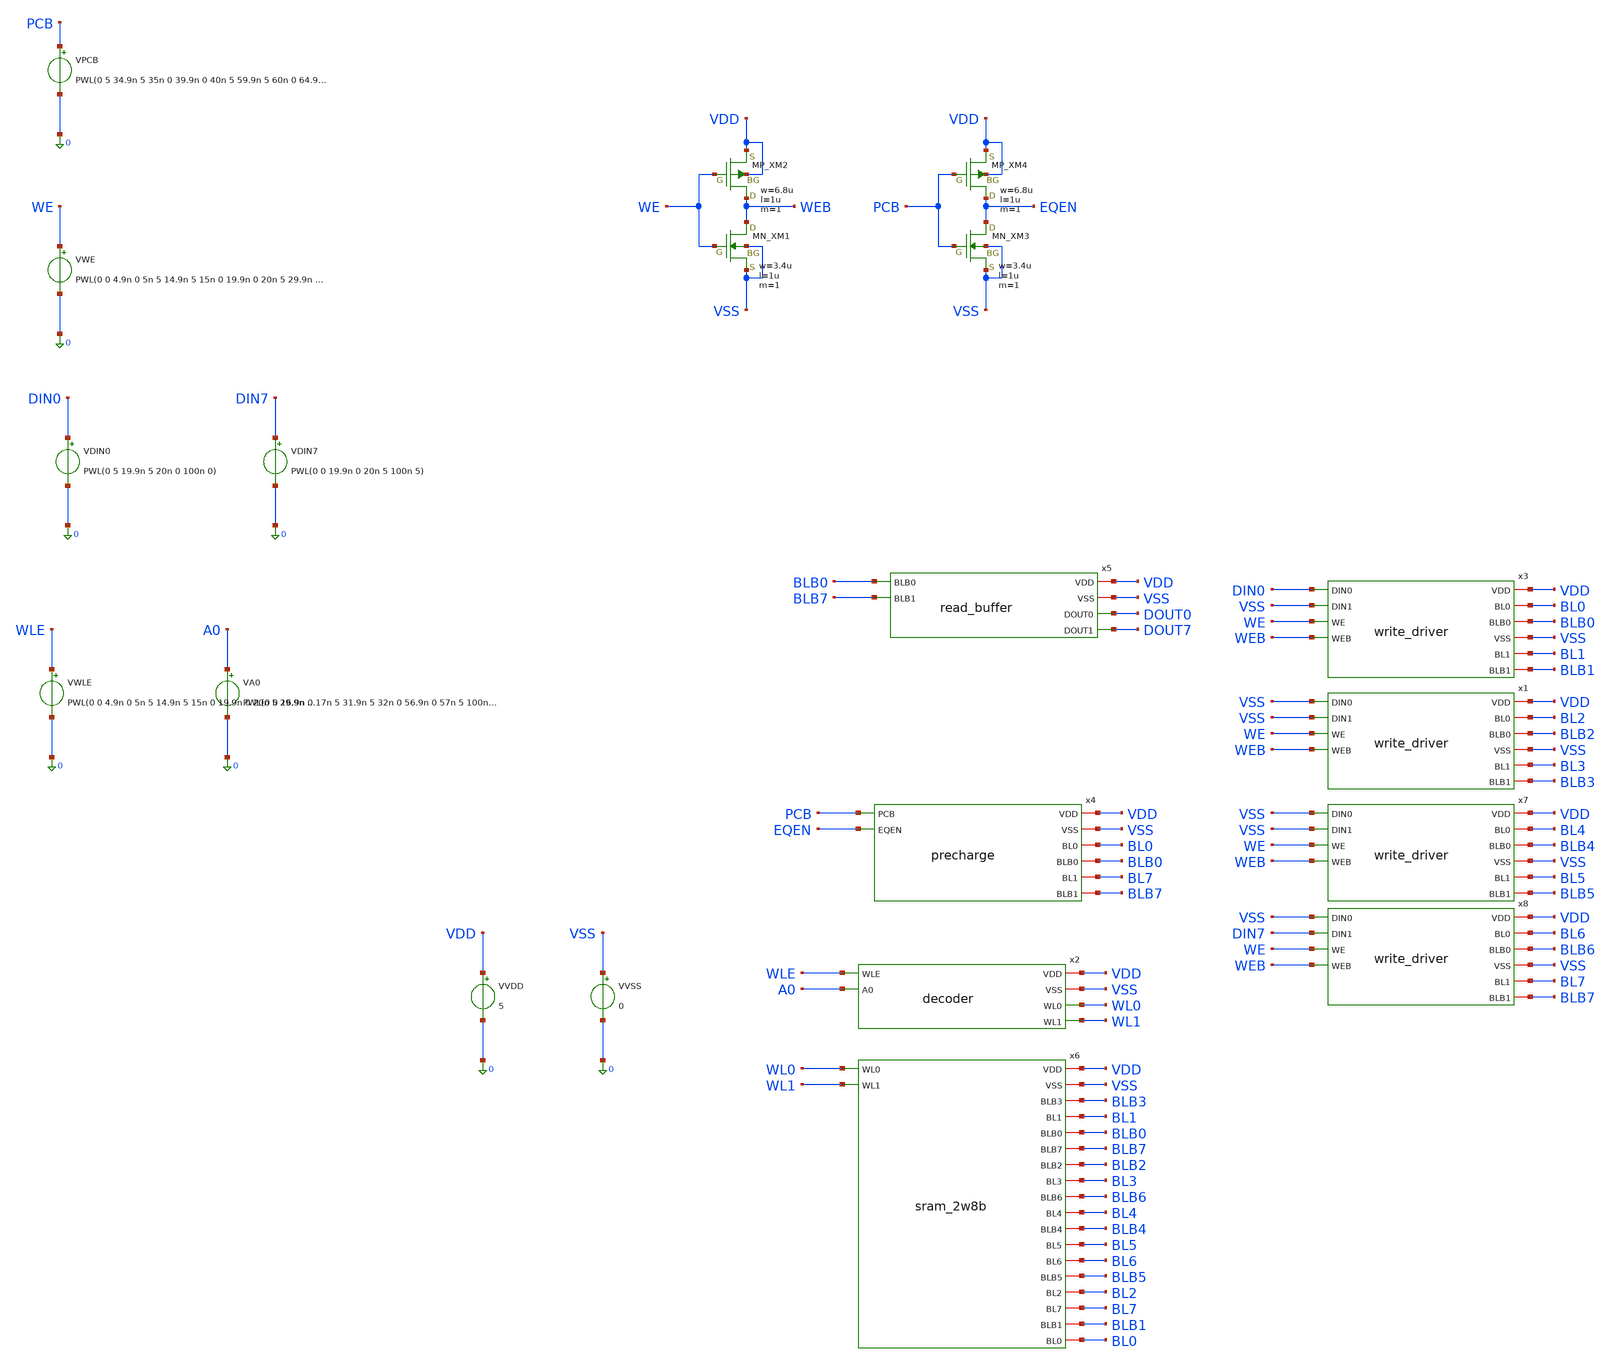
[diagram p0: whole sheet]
** sch_path: sram/tb_sram_2w8b.sch
**.subckt tb_sram_2w8b
VVDD VDD 0 5
VDIN0 DIN0 0 PWL(0 5 19.9n 5 20n 0 100n 0)
VVSS VSS 0 0
VWE WE 0 PWL(0 0 4.9n 0 5n 5 14.9n 5 15n 0 19.9n 0 20n 5 29.9n 5 30n 0 100n 0)
VPCB PCB 0 PWL(0 5 34.9n 5 35n 0 39.9n 0 40n 5 59.9n 5 60n 0 64.9n 0 65n 5 100n 5)
x2 VDD VSS WL0 WLE A0 WL1 decoder
VWLE WLE 0 PWL(0 0 4.9n 0 5n 5 14.9n 5 15n 0 19.9n 0 20n 5 29.9n 5 30n 0 44.9n 0 45n 5 54.9n 5 55n 0
+ 69.9n 0 70n 5 79.9n 5 80n 0 100n 0)
VA0 A0 0 PWL(0 0 16.9n 0 17n 5 31.9n 5 32n 0 56.9n 0 57n 5 100n 5)
x3 DIN0 VDD BL0 BLB0 VSS VSS BL1 WE BLB1 WEB write_driver
VDIN7 DIN7 0 PWL(0 0 19.9n 0 20n 5 100n 5)
x4 VDD VSS PCB EQEN BL0 BLB0 BL7 BLB7 precharge
x5 VDD VSS BLB0 BLB7 DOUT0 DOUT7 read_buffer
XXM1 WEB WE VSS VSS NMOS w=3.4u l=1u nrd=0 nrs=0 m=1
XXM2 WEB WE VDD VDD PMOS w=6.8u l=1u nrd=0 nrs=0 m=1
XXM3 EQEN PCB VSS VSS NMOS w=3.4u l=1u nrd=0 nrs=0 m=1
XXM4 EQEN PCB VDD VDD PMOS w=6.8u l=1u nrd=0 nrs=0 m=1
x6 WL0 VDD VSS WL1 BLB3 BL1 BLB0 BLB7 BLB2 BL3 BLB6 BL4 BLB4 BL5 BL6 BLB5 BL2 BL7 BLB1 BL0 sram_2w8b
x1 VSS VDD BL2 BLB2 VSS VSS BL3 WE BLB3 WEB write_driver
x7 VSS VDD BL4 BLB4 VSS VSS BL5 WE BLB5 WEB write_driver
x8 VSS VDD BL6 BLB6 VSS DIN7 BL7 WE BLB7 WEB write_driver
**** begin user architecture code
 .include $::LIB/ip62_models


.tran 10p 100n

* ============================================================
* ColMax 2w8b SRAM Read Measurement
* Observe: bit1 and bit7
* ============================================================

* WL 50% crossing
.meas tran t_wl0_rise WHEN v(WL0)=2.5 RISE=2
.meas tran t_wl1_rise WHEN v(WL1)=2.5 RISE=1

* BL differential at WL0 +0.5ns
.meas tran dvbl0_05 FIND par('abs(v(BL0)-v(BLB0))') AT=47.781n
.meas tran dvbl7_05 FIND par('abs(v(BL7)-v(BLB7))') AT=47.781n

* BL differential at WL0 +1.0ns
.meas tran dvbl0_10 FIND par('abs(v(BL0)-v(BLB0))') AT=48.281n
.meas tran dvbl7_10 FIND par('abs(v(BL7)-v(BLB7))') AT=48.281n

* Time when BL differential reaches 1.0V
.meas tran t_dvbl0_1v WHEN par('abs(v(BL0)-v(BLB0))')=1.0 RISE=1 TD=47n
.meas tran t_dvbl7_1v WHEN par('abs(v(BL7)-v(BLB7))')=1.0 RISE=1 TD=47n

* Delay from WL0 50% to 1.0V BL differential
.meas tran td_bl0 PARAM='t_dvbl0_1v-t_wl0_rise'
.meas tran td_bl7 PARAM='t_dvbl7_1v-t_wl0_rise'

.control
run
plot v(pcb) v(eqen)+6
plot v(wl0) v(wl1)+6
plot v(dout0) v(dout7)+6
plot v(bl0) v(blb0)
plot v(bl7) v(blb7)


.endc


**** end user architecture code
**.ends
.end
